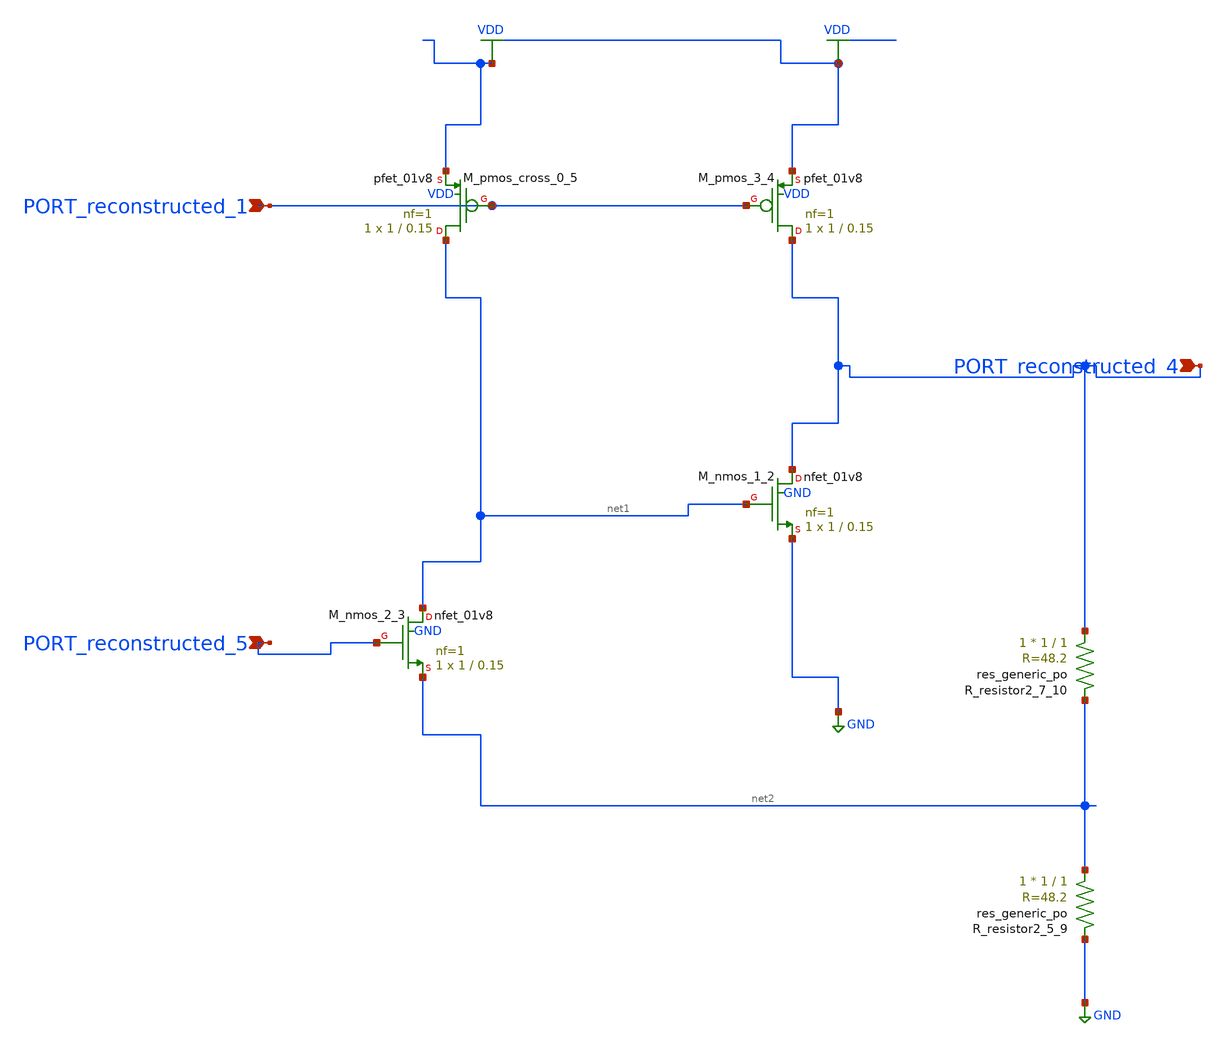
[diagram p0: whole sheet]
** sch_path: schematics/AMSNet/617.sch
**.subckt 617 PORT_reconstructed_4 PORT_reconstructed_5 PORT_reconstructed_1
*.ipin PORT_reconstructed_4
*.ipin PORT_reconstructed_5
*.ipin PORT_reconstructed_1
XM_nmos_1_2 PORT_reconstructed_4 net1 GND GND sky130_fd_pr__nfet_01v8 L=0.15 W=1 nf=1 ad='int((1 + 1)/2) * 1 / 1 * 0.29'
+ as='int((1 + 2)/2) * 1 / 1 * 0.29' pd='2*int((1 + 1)/2) * (1 / 1 + 0.29)' ps='2*int((1 + 2)/2) * (1 / 1 + 0.29)'
+ nrd='0.29 / 1 ' nrs='0.29 / 1 ' sa=0 sb=0 sd=0 mult=1 m=1
XM_nmos_2_3 net1 PORT_reconstructed_5 net2 GND sky130_fd_pr__nfet_01v8 L=0.15 W=1 nf=1 ad='int((1 + 1)/2) * 1 / 1 * 0.29'
+ as='int((1 + 2)/2) * 1 / 1 * 0.29' pd='2*int((1 + 1)/2) * (1 / 1 + 0.29)' ps='2*int((1 + 2)/2) * (1 / 1 + 0.29)'
+ nrd='0.29 / 1 ' nrs='0.29 / 1 ' sa=0 sb=0 sd=0 mult=1 m=1
XM_pmos_3_4 PORT_reconstructed_4 PORT_reconstructed_1 VDD VDD sky130_fd_pr__pfet_01v8 L=0.15 W=1 nf=1
+ ad='int((1 + 1)/2) * 1 / 1 * 0.29' as='int((1 + 2)/2) * 1 / 1 * 0.29' pd='2*int((1 + 1)/2) * (1 / 1 + 0.29)'
+ ps='2*int((1 + 2)/2) * (1 / 1 + 0.29)' nrd='0.29 / 1 ' nrs='0.29 / 1 ' sa=0 sb=0 sd=0 mult=1 m=1
XM_pmos_cross_0_5 net1 PORT_reconstructed_1 VDD VDD sky130_fd_pr__pfet_01v8 L=0.15 W=1 nf=1 ad='int((1 + 1)/2) * 1 / 1 * 0.29'
+ as='int((1 + 2)/2) * 1 / 1 * 0.29' pd='2*int((1 + 1)/2) * (1 / 1 + 0.29)' ps='2*int((1 + 2)/2) * (1 / 1 + 0.29)'
+ nrd='0.29 / 1 ' nrs='0.29 / 1 ' sa=0 sb=0 sd=0 mult=1 m=1
XR_resistor2_5_9 net2 GND sky130_fd_pr__res_generic_po W=1 L=1 m=1
XR_resistor2_7_10 PORT_reconstructed_4 net2 sky130_fd_pr__res_generic_po W=1 L=1 m=1
**.ends
.GLOBAL GND
.GLOBAL VDD
.end
